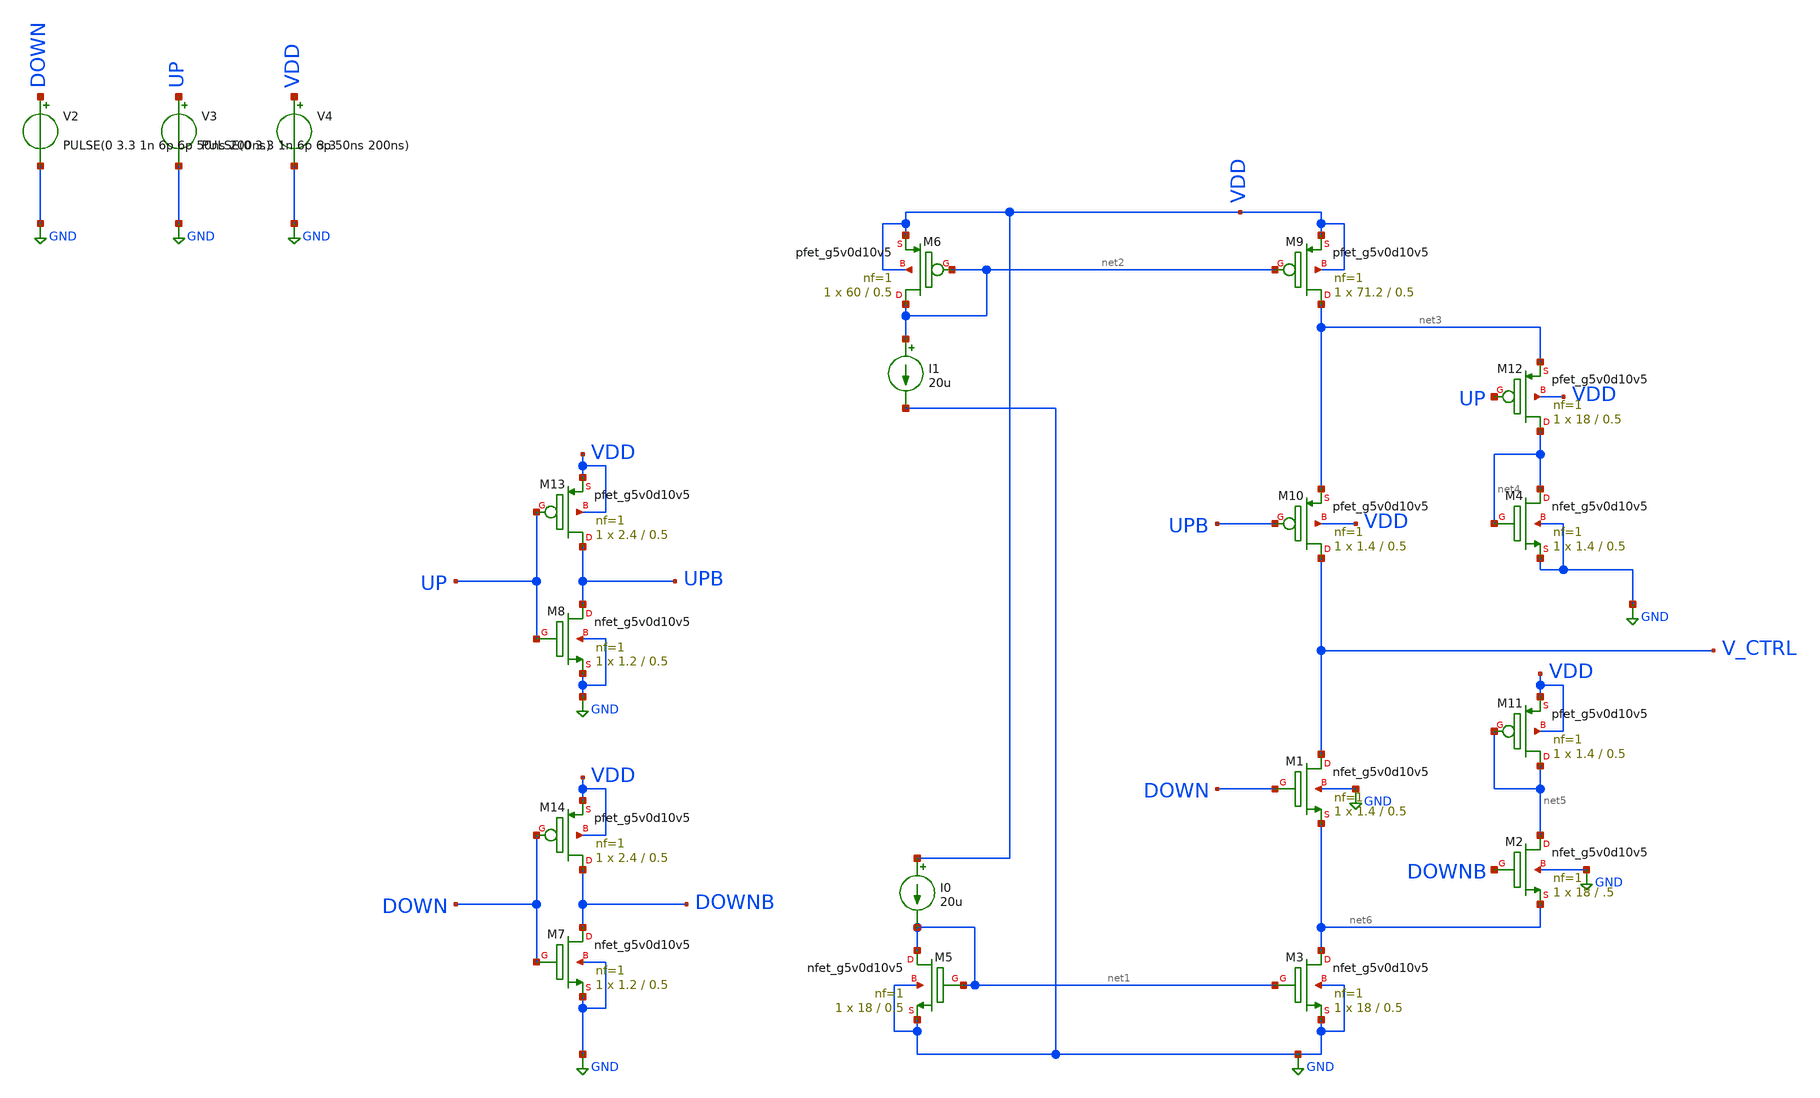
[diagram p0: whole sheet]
** sch_path: ChargePump_LoopFilter/03_test_CP_v3.sch
**.subckt 03_test_CP_v3
V2 DOWN GND PULSE(0 3.3 1n 6p 6p 50ns 200ns)
V3 UP GND PULSE(0 3.3 1n 6p 6p 50ns 200ns)
V4 VDD GND 3.3
XM1 V_CTRL DOWN net6 GND sky130_fd_pr__nfet_g5v0d10v5 L=0.5 W=1.4 nf=1 ad='int((nf+1)/2) * W/nf * 0.29'
+ as='int((nf+2)/2) * W/nf * 0.29' pd='2*int((nf+1)/2) * (W/nf + 0.29)' ps='2*int((nf+2)/2) * (W/nf + 0.29)'
+ nrd='0.29 / W' nrs='0.29 / W' sa=0 sb=0 sd=0 mult=1 m=1
XM2 net5 DOWNB net6 GND sky130_fd_pr__nfet_g5v0d10v5 L=.5 W=18 nf=1 ad='int((nf+1)/2) * W/nf * 0.29'
+ as='int((nf+2)/2) * W/nf * 0.29' pd='2*int((nf+1)/2) * (W/nf + 0.29)' ps='2*int((nf+2)/2) * (W/nf + 0.29)'
+ nrd='0.29 / W' nrs='0.29 / W' sa=0 sb=0 sd=0 mult=1 m=1
XM3 net6 net1 GND GND sky130_fd_pr__nfet_g5v0d10v5 L=0.5 W=18 nf=1 ad='int((nf+1)/2) * W/nf * 0.29' as='int((nf+2)/2) * W/nf * 0.29'
+ pd='2*int((nf+1)/2) * (W/nf + 0.29)' ps='2*int((nf+2)/2) * (W/nf + 0.29)' nrd='0.29 / W' nrs='0.29 / W'
+ sa=0 sb=0 sd=0 mult=1 m=1
XM4 net4 net4 GND GND sky130_fd_pr__nfet_g5v0d10v5 L=0.5 W=1.4 nf=1 ad='int((nf+1)/2) * W/nf * 0.29'
+ as='int((nf+2)/2) * W/nf * 0.29' pd='2*int((nf+1)/2) * (W/nf + 0.29)' ps='2*int((nf+2)/2) * (W/nf + 0.29)'
+ nrd='0.29 / W' nrs='0.29 / W' sa=0 sb=0 sd=0 mult=1 m=1
XM5 net1 net1 GND GND sky130_fd_pr__nfet_g5v0d10v5 L=0.5 W=18 nf=1 ad='int((nf+1)/2) * W/nf * 0.29' as='int((nf+2)/2) * W/nf * 0.29'
+ pd='2*int((nf+1)/2) * (W/nf + 0.29)' ps='2*int((nf+2)/2) * (W/nf + 0.29)' nrd='0.29 / W' nrs='0.29 / W'
+ sa=0 sb=0 sd=0 mult=1 m=1
XM7 DOWNB DOWN GND GND sky130_fd_pr__nfet_g5v0d10v5 L=0.5 W=1.2 nf=1 ad='int((nf+1)/2) * W/nf * 0.29'
+ as='int((nf+2)/2) * W/nf * 0.29' pd='2*int((nf+1)/2) * (W/nf + 0.29)' ps='2*int((nf+2)/2) * (W/nf + 0.29)'
+ nrd='0.29 / W' nrs='0.29 / W' sa=0 sb=0 sd=0 mult=1 m=1
XM8 UPB UP GND GND sky130_fd_pr__nfet_g5v0d10v5 L=0.5 W=1.2 nf=1 ad='int((nf+1)/2) * W/nf * 0.29' as='int((nf+2)/2) * W/nf * 0.29'
+ pd='2*int((nf+1)/2) * (W/nf + 0.29)' ps='2*int((nf+2)/2) * (W/nf + 0.29)' nrd='0.29 / W' nrs='0.29 / W'
+ sa=0 sb=0 sd=0 mult=1 m=1
XM6 net2 net2 VDD VDD sky130_fd_pr__pfet_g5v0d10v5 L=0.5 W=60 nf=1 ad='int((nf+1)/2) * W/nf * 0.29' as='int((nf+2)/2) * W/nf * 0.29'
+ pd='2*int((nf+1)/2) * (W/nf + 0.29)' ps='2*int((nf+2)/2) * (W/nf + 0.29)' nrd='0.29 / W' nrs='0.29 / W'
+ sa=0 sb=0 sd=0 mult=1 m=1
XM9 net3 net2 VDD VDD sky130_fd_pr__pfet_g5v0d10v5 L=0.5 W=71.2 nf=1 ad='int((nf+1)/2) * W/nf * 0.29'
+ as='int((nf+2)/2) * W/nf * 0.29' pd='2*int((nf+1)/2) * (W/nf + 0.29)' ps='2*int((nf+2)/2) * (W/nf + 0.29)'
+ nrd='0.29 / W' nrs='0.29 / W' sa=0 sb=0 sd=0 mult=1 m=1
XM10 V_CTRL UPB net3 VDD sky130_fd_pr__pfet_g5v0d10v5 L=0.5 W=1.4 nf=1 ad='int((nf+1)/2) * W/nf * 0.29'
+ as='int((nf+2)/2) * W/nf * 0.29' pd='2*int((nf+1)/2) * (W/nf + 0.29)' ps='2*int((nf+2)/2) * (W/nf + 0.29)'
+ nrd='0.29 / W' nrs='0.29 / W' sa=0 sb=0 sd=0 mult=1 m=1
XM11 net5 net5 VDD VDD sky130_fd_pr__pfet_g5v0d10v5 L=0.5 W=1.4 nf=1 ad='int((nf+1)/2) * W/nf * 0.29'
+ as='int((nf+2)/2) * W/nf * 0.29' pd='2*int((nf+1)/2) * (W/nf + 0.29)' ps='2*int((nf+2)/2) * (W/nf + 0.29)'
+ nrd='0.29 / W' nrs='0.29 / W' sa=0 sb=0 sd=0 mult=1 m=1
XM12 net4 UP net3 VDD sky130_fd_pr__pfet_g5v0d10v5 L=0.5 W=18 nf=1 ad='int((nf+1)/2) * W/nf * 0.29' as='int((nf+2)/2) * W/nf * 0.29'
+ pd='2*int((nf+1)/2) * (W/nf + 0.29)' ps='2*int((nf+2)/2) * (W/nf + 0.29)' nrd='0.29 / W' nrs='0.29 / W'
+ sa=0 sb=0 sd=0 mult=1 m=1
XM13 UPB UP VDD VDD sky130_fd_pr__pfet_g5v0d10v5 L=0.5 W=2.4 nf=1 ad='int((nf+1)/2) * W/nf * 0.29' as='int((nf+2)/2) * W/nf * 0.29'
+ pd='2*int((nf+1)/2) * (W/nf + 0.29)' ps='2*int((nf+2)/2) * (W/nf + 0.29)' nrd='0.29 / W' nrs='0.29 / W'
+ sa=0 sb=0 sd=0 mult=1 m=1
XM14 DOWNB DOWN VDD VDD sky130_fd_pr__pfet_g5v0d10v5 L=0.5 W=2.4 nf=1 ad='int((nf+1)/2) * W/nf * 0.29'
+ as='int((nf+2)/2) * W/nf * 0.29' pd='2*int((nf+1)/2) * (W/nf + 0.29)' ps='2*int((nf+2)/2) * (W/nf + 0.29)'
+ nrd='0.29 / W' nrs='0.29 / W' sa=0 sb=0 sd=0 mult=1 m=1
I0 VDD net1 20u
I1 net2 GND 20u
**** begin user architecture code


.lib /home/huydq/pdk/sky130A/libs.tech/ngspice/sky130.lib.spice.tt.red tt
.ic v(out) = 0
.control
save all
*save @m.xm2.msky130_fd_pr__pfet_01v8[gm]
*save @m.xm2.msky130_fd_pr__pfet_01v8[vth]
*op
tran 1n 200u
*noise v(out) V2 dec 10 1kHz 100MEG
*dc V2 0 1.2 0.01
plot v(out) c(out)
*print v(A) {v(CLK)+2}
*print @m.xm2.msky130_fd_pr__pfet_01v8
write 04_test_CP_v2.raw
quit 0
.endc

**** end user architecture code
**.ends
.GLOBAL GND
.end
